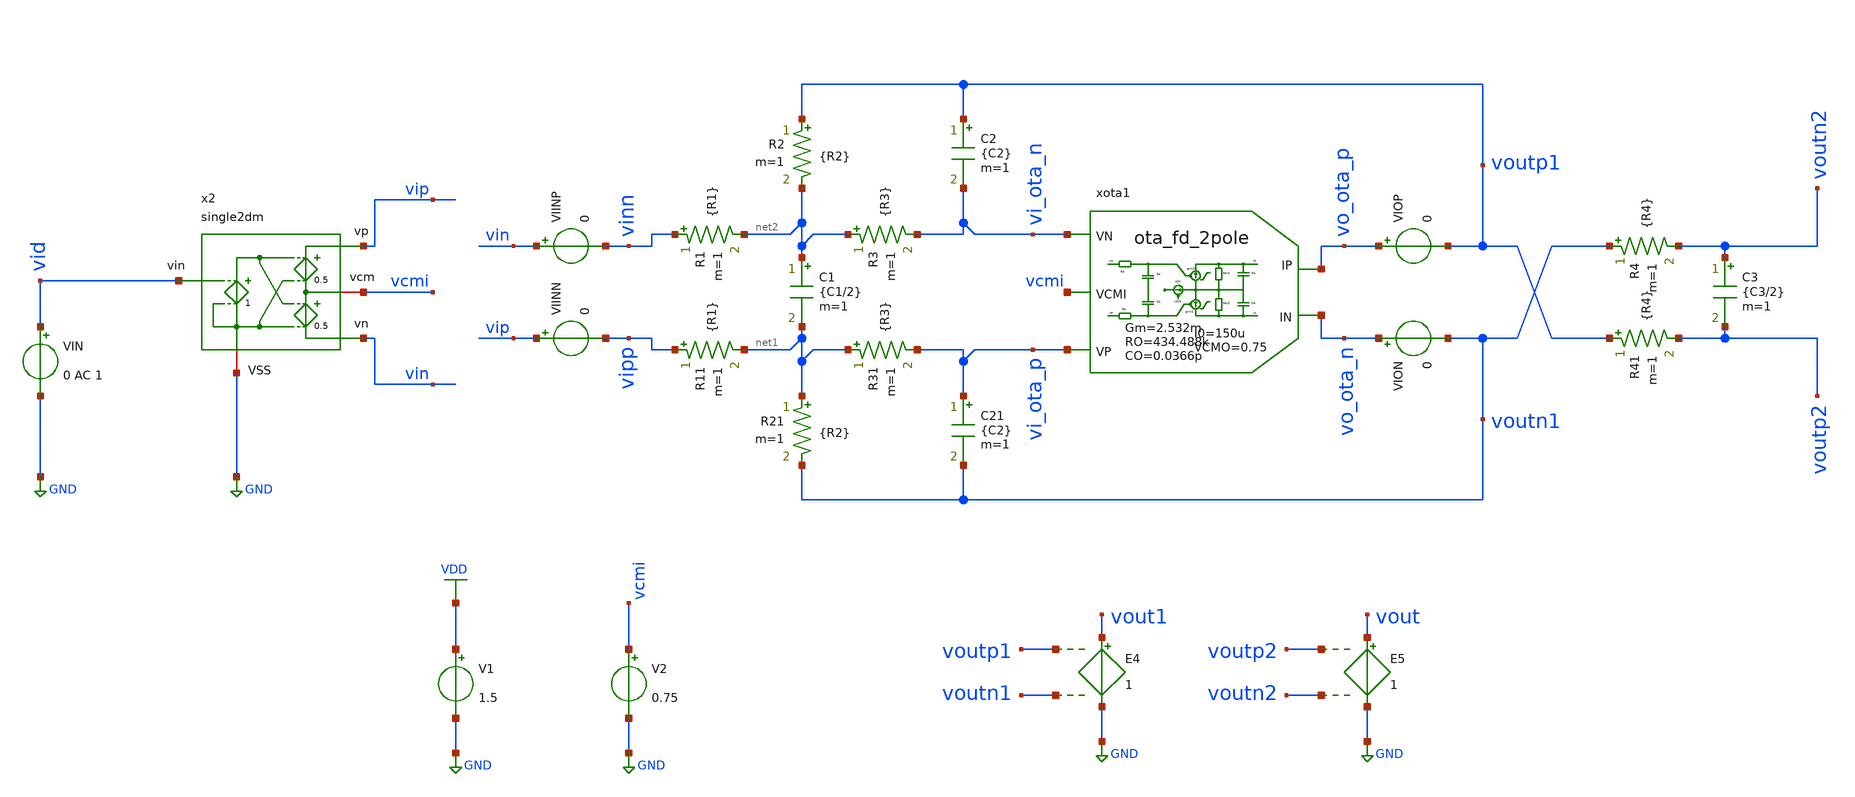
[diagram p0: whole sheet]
** sch_path: macros/filter_cmos5l/testbenches/xschem/filter_cl_ideal_tb_param.sch
**.subckt filter_cl_ideal_tb_param
VIN vid GND 0 AC 1
E4 vout1 GND voutp1 voutn1 1
VIINP vin vinn 0
VIINN vip vipp 0
R1 vinn net2 {R1} m=1
R2 voutp1 net2 {R2} m=1
R3 net2 vi_ota_n {R3} m=1
C1 net2 net1 {C1/2} m=1
C3 voutn2 voutp2 {C3/2} m=1
R11 vipp net1 {R1} m=1
R21 net1 voutn1 {R2} m=1
R31 net1 vi_ota_p {R3} m=1
C21 vi_ota_p voutn1 {C2} m=1
R4 voutn1 voutn2 {R4} m=1
R41 voutp1 voutp2 {R4} m=1
C2 voutp1 vi_ota_n {C2} m=1
E5 vout GND voutp2 voutn2 1
VIOP vo_ota_p voutp1 0
VION vo_ota_n voutn1 0
V1 VDD GND 1.5
x2 vip vid vcmi GND vin single2dm
V2 vcmi GND 0.75
xota1 vi_ota_n vo_ota_p vo_ota_n vi_ota_p vcmi ota_fd_2pole GM=2.532m RO=434.488k CO=0.0366p RP=0
+ CP=0.01f VCMO=0.75 I0=150u
**** begin user architecture code


.include /foss/designs/kvosid_336004_ss26/macros/filter_cmos5l/scripts/sizing/filterPassives.spice
.options savecurrents
.options method=gear reltol=.005
.options sparse
.control
save all

let f_min = 10
let f_max = 100Meg
let f_stop = 9Meg
let f_nmin = 100
let f_nmax = 5Meg

let n_bits = 8
let Adc = 10
let v_fs = 1.0
let v_lsb = v_fs/2^n_bits
let v_qn = v_lsb/sqrt(12)
let err_gain_spec = v_lsb/v_fs
let vo_n_max = 113e-6

let v_step_o = v_fs
let v_step_i = v_step_o/Adc

let t_rf = 0.1u
let t_step = 50u
let t_delay = 0
let t_per = 2*t_step

let tstep = 0.1*t_rf
let tstop = 2*t_per
let tstart = t_delay

*alter @VIN[SIN] = [ 0 0.01 $&f_sig 0 0 0 ]
alter @VIN[DC] = 0.0

set wr_singlescale
set wr_vecnames
option numdgt=3

set opSimOnly = 0


** Main Simulations
if $opSimOnly eq 0
	op
	ac dec 100 $&const.f_min $&const.f_max
	*set sqrnoise
	noise v(vout) VIN dec 100 $&const.f_min $&const.f_max 1
	noise v(vout) VIN dec 10 $&const.f_nmin $&const.f_nmax
	alter @VIN[PULSE] = [ 0 $&v_step_i $&t_delay $&t_rf $&t_rf $&t_step $&t_per 0 ]
	** Check power on by ramping Vdd, tie di_pon to VDD net!
	*alter @V1[PULSE] = [ 0 1.8 0 10u $&t_rf 0 0 0 ]
	tran $&tstep $&tstop $&tstart

	setplot ac1
	let A1 = v(vout1)/v(vid)
	let A2 = v(vout)/v(vid)

	let Amag_dB = vdb(A2)
	settype decibel Amag_dB
	let Aarg = 180/PI*cphase(A2)

	let fdc = const.f_min+1
	meas ac Adc_ol_dB find Amag_dB when frequency = fdc
	let Amag_fc = Adc_ol_dB-3
	meas ac fc find frequency when Amag_dB = Amag_fc
	meas ac Amin min_at Amag_dB from=const.f_min to=fc
	meas ac Amax max Amag_dB
	meas ac Astop find Amag_dB when frequency = const.f_stop
	let att_db = Adc_ol_dB-Astop

	meas ac fug find frequency when Amag_dB=0
	let err_gain_act = 1-10^(Adc_ol_dB/20)/Adc
	let Adc_ol_min = (1+Adc)*(1-err_gain_spec)/err_gain_spec
	let Adc_ol_min_dB = vdb(Adc_ol_min)
	print err_gain_act*100
	print Adc_ol_min_dB
	print att_db
	wrdata ../plot_simulations/data/filter_cl_ideal_tb_ac.txt Amag_dB Aarg
	plot Amag_dB Aarg ylabel 'Magnitude, Phase'

	setplot noise3
	wrdata ../plot_simulations/data/filter_cl_ideal_tb_noise.txt onoise_spectrum

	setplot noise4
	let p_noise_q = const.v_qn^2
	let p_noise_o = onoise_total^2
	let p_sig_o = (v_step_o/(2*sqrt(2)))^2
	let snr = p_sig_o/(p_noise_o+p_noise_q)
	let snr_dB = 10*log10(snr)
	print snr_dB

	setplot tran4
	let vid = v(vid)
	let iop = viop#branch
	let ion = vion#branch
	let vcmo = (voutp1+voutn1)/2

	*plot iop ion

	*plot vid vout1 vout vcmo
	*plot v(vip) v(vin) v(voutp1) v(voutn1) vcmo
end

alter @VIN[DC] = 0
op

remzerovec
write filter_cl_ideal_tb.raw
.endc

**** end user architecture code
**.ends

* expanding   symbol:  single2dm.sym # of pins=5
** sym_path: single2dm.sym
** sch_path: single2dm.sch
.subckt single2dm vp vin vcm VSS vn
*.ipin vin
*.opin vn
*.iopin vcm
*.opin vp
*.iopin VSS
E3 vcm vn net1 VSS 0.5
E2 vp vcm net1 VSS 0.5
E1 net1 VSS vin VSS 1
.ends


* expanding   symbol:  ota_fd_2pole.sym # of pins=5
** sym_path: ota_fd_2pole.sym
** sch_path: ota_fd_2pole.sch
.subckt ota_fd_2pole VN IP IN VP VCMI  GM=1u RO=100Meg CO=1p RP=0 CP=0.1p VCMO=0 I0=1u
*.ipin VP
*.ipin VN
*.opin IP
*.opin IN
*.ipin VCMI
R3 IP net1 {RO/2} m=1
R4 IN net1 {RO/2} m=1
C3 IP net1 {CO} m=1
R5 VN ip1 {RP} m=1
C4 ip1 VCMI {CP} m=1
C6 in1 VCMI {CP} m=1
C8 IN net1 {CO} m=1
R7 VP in1 {RP} m=1
B2 IP net1 I = {I0*tanh(GM/2*V(ip1,in1)/I0)}
B1 net1 IN I = {I0*tanh(GM/2*V(ip1,in1)/I0)}
B5 net1 GND I = {VCMO-(V(IP)+V(IN))/2}
.ends

.GLOBAL GND
.GLOBAL VDD
.end
